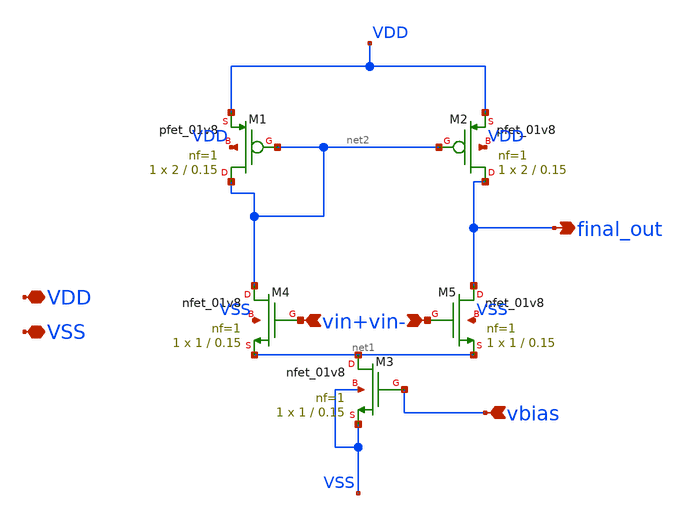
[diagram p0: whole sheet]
** sch_path: xschem/attic/D2S_amp.sch
**.subckt D2S_amp VDD VSS final_out vin+ vin- vbias
*.iopin VDD
*.iopin VSS
*.opin final_out
*.ipin vin+
*.ipin vin-
*.ipin vbias
XM1 net2 net2 VDD VDD sky130_fd_pr__pfet_01v8 L=0.15 W=2 nf=1 ad='int((nf+1)/2) * W/nf * 0.29' as='int((nf+2)/2) * W/nf * 0.29'
+ pd='2*int((nf+1)/2) * (W/nf + 0.29)' ps='2*int((nf+2)/2) * (W/nf + 0.29)' nrd='0.29 / W' nrs='0.29 / W'
+ sa=0 sb=0 sd=0 mult=1 m=1
XM2 final_out net2 VDD VDD sky130_fd_pr__pfet_01v8 L=0.15 W=2 nf=1 ad='int((nf+1)/2) * W/nf * 0.29' as='int((nf+2)/2) * W/nf * 0.29'
+ pd='2*int((nf+1)/2) * (W/nf + 0.29)' ps='2*int((nf+2)/2) * (W/nf + 0.29)' nrd='0.29 / W' nrs='0.29 / W'
+ sa=0 sb=0 sd=0 mult=1 m=1
XM4 net2 vin+ net1 VSS sky130_fd_pr__nfet_01v8 L=0.15 W=1 nf=1 ad='int((nf+1)/2) * W/nf * 0.29' as='int((nf+2)/2) * W/nf * 0.29'
+ pd='2*int((nf+1)/2) * (W/nf + 0.29)' ps='2*int((nf+2)/2) * (W/nf + 0.29)' nrd='0.29 / W' nrs='0.29 / W'
+ sa=0 sb=0 sd=0 mult=1 m=1
XM5 final_out vin- net1 VSS sky130_fd_pr__nfet_01v8 L=0.15 W=1 nf=1 ad='int((nf+1)/2) * W/nf * 0.29'
+ as='int((nf+2)/2) * W/nf * 0.29' pd='2*int((nf+1)/2) * (W/nf + 0.29)' ps='2*int((nf+2)/2) * (W/nf + 0.29)'
+ nrd='0.29 / W' nrs='0.29 / W' sa=0 sb=0 sd=0 mult=1 m=1
XM3 net1 vbias VSS VSS sky130_fd_pr__nfet_01v8 L=0.15 W=1 nf=1 ad='int((nf+1)/2) * W/nf * 0.29' as='int((nf+2)/2) * W/nf * 0.29'
+ pd='2*int((nf+1)/2) * (W/nf + 0.29)' ps='2*int((nf+2)/2) * (W/nf + 0.29)' nrd='0.29 / W' nrs='0.29 / W'
+ sa=0 sb=0 sd=0 mult=1 m=1
**.ends
.end
